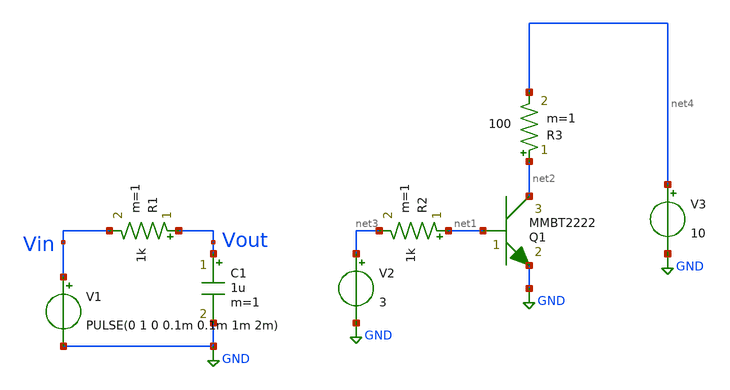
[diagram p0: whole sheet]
** sch_path: tests.sch
**.subckt tests
R1 Vout Vin 1k m=1
C1 Vout GND 1u m=1
V1 Vin GND PULSE(0 1 0 0.1m 0.1m 1m 2m)
Q1 net2 net1 GND MMBT2222 area=1 m=1
R2 net1 net3 1k m=1
R3 net2 net4 100 m=1
V2 net3 GND 3
V3 net4 GND 10
**** begin user architecture code


.tran 1u 10m
.save all


**** end user architecture code
**.ends
.GLOBAL GND
.end
